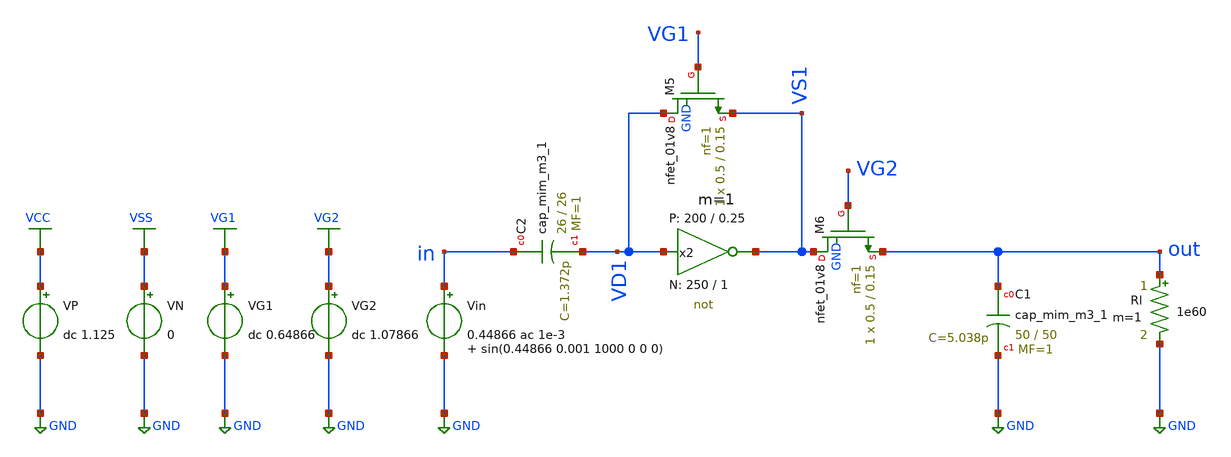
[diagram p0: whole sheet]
** sch_path: Amplifier_Inv/xschem/v3/DC_tb_v3.sch
* StefanSchippers/xschem_sky130/sky130_tests/not.sch:
* Copyright 2021 Stefan Frederik Schippers
* Licensed under the Apache License, Version 2.0 (the "License");
**.subckt DC_tb_v3
Vin in GND 0.44866 ac 1e-3 sin(0.44866 0.001 1000 0 0 0)
Rl out GND 1e60 m=1
x2 VS1 VD1 VCC VSS not W_N=250 L_N=1 W_P=200 L_P=0.25 m=1
XC1 out GND sky130_fd_pr__cap_mim_m3_1 W=50 L=50 MF=1 m=1
XM5 VD1 VG1 VS1 GND sky130_fd_pr__nfet_01v8 L=0.15 W=0.5 nf=1 ad='int((nf+1)/2) * W/nf * 0.29' as='int((nf+2)/2) * W/nf * 0.29'
+ pd='2*int((nf+1)/2) * (W/nf + 0.29)' ps='2*int((nf+2)/2) * (W/nf + 0.29)' nrd='0.29 / W' nrs='0.29 / W'
+ sa=0 sb=0 sd=0 mult=1 m=1
XM6 VS1 VG2 out GND sky130_fd_pr__nfet_01v8 L=0.15 W=0.5 nf=1 ad='int((nf+1)/2) * W/nf * 0.29' as='int((nf+2)/2) * W/nf * 0.29'
+ pd='2*int((nf+1)/2) * (W/nf + 0.29)' ps='2*int((nf+2)/2) * (W/nf + 0.29)' nrd='0.29 / W' nrs='0.29 / W'
+ sa=0 sb=0 sd=0 mult=1 m=1
VN VSS GND 0
VP VCC GND dc 1.125
VG2 VG2 GND dc 1.07866
VG1 VG1 GND dc 0.64866
XC2 in VD1 sky130_fd_pr__cap_mim_m3_1 W=26 L=26 MF=1 m=1
**** begin user architecture code

** opencircuitdesign pdks install
.lib $::SKYWATER_MODELS/sky130.lib.spice tt



.control

  dc Vin 0 1.125 0.00001
  save all v(out) v(vg1) v(vg2) v(vs1) v(vd1)
  write tb_inv_sky130_a_DC_v3.raw v(out) v(vg1) v(vg2) v(vs1) v(vd1)



  exit 0
.endc


**** end user architecture code
**.ends

* expanding   symbol:  sky130_tests/not.sym # of pins=2
** sym_path: sky130_tests/not.sym
** sch_path: sky130_tests/not.sch
.subckt not y a VCCPIN VSSPIN     W_N=1 L_N=0.15 W_P=2 L_P=0.15
*.opin y
*.ipin a
XM1 DN a VSSPIN VSSPIN sky130_fd_pr__nfet_01v8 L=L_N W=W_N nf=1 ad='int((1 + 1)/2) * W_N / 1 * 0.29'
+ as='int((1 + 2)/2) * W_N / 1 * 0.29' pd='2*int((1 + 1)/2) * (W_N / 1 + 0.29)' ps='2*int((1 + 2)/2) * (W_N / 1 + 0.29)'
+ nrd='0.29 / W_N ' nrs='0.29 / W_N ' sa=0 sb=0 sd=0 mult=1 m=1
XM2 DP a VCCPIN VCCPIN sky130_fd_pr__pfet_01v8 L=L_P W=W_P nf=1 ad='int((nf+1)/2) * W/nf * 0.29' as='int((nf+2)/2) * W/nf * 0.29'
+ pd='2*int((nf+1)/2) * (W/nf + 0.29)' ps='2*int((nf+2)/2) * (W/nf + 0.29)' nrd='0.29 / W' nrs='0.29 / W'
+ sa=0 sb=0 sd=0 mult=1 m=1
Vmeas DP y 0
.save i(vmeas)
Vmeas1 y DN 0
.save i(vmeas1)
.save v(dp)
.save v(dn)
.ends

.GLOBAL GND
.GLOBAL VSS
.GLOBAL VCC
.GLOBAL VG2
.GLOBAL VG1
.end
